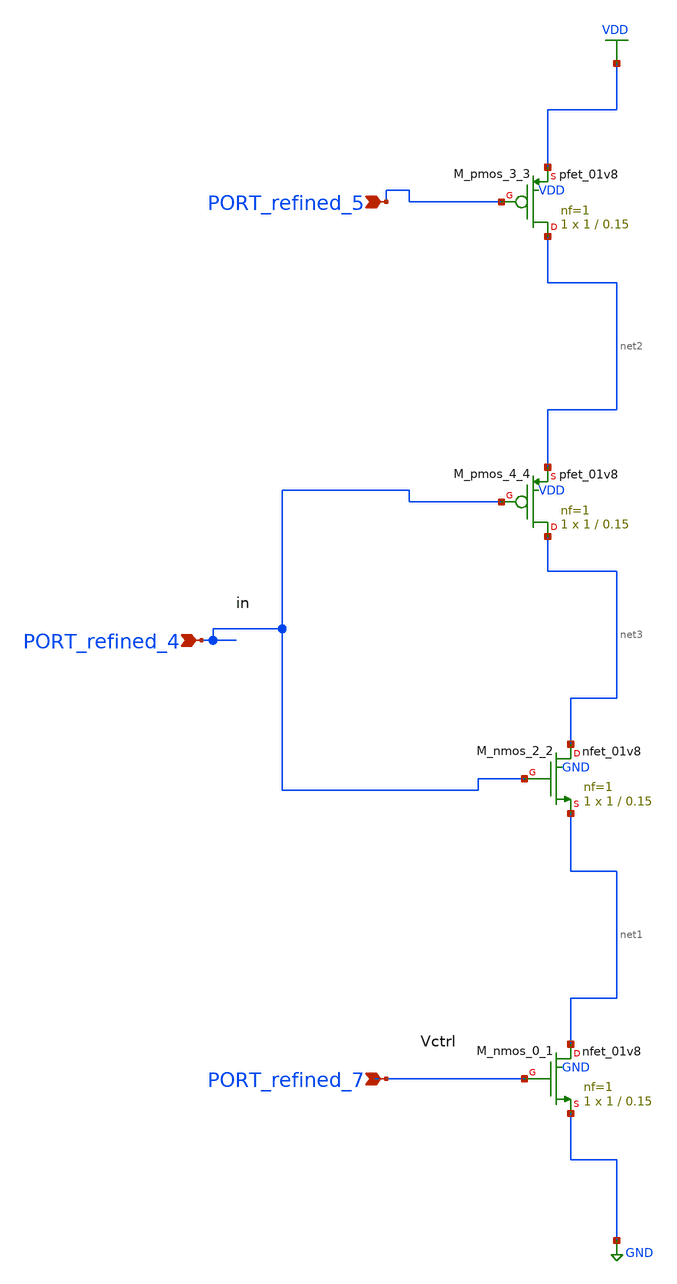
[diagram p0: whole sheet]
** sch_path: schematics/10_1109_ACCESS_2019_2905767_06_001_crop1.sch
**.subckt 10_1109_ACCESS_2019_2905767_06_001_crop1 PORT_refined_5 PORT_refined_4 PORT_refined_7
*.ipin PORT_refined_5
*.ipin PORT_refined_4
*.ipin PORT_refined_7
XM_nmos_0_1 net1 PORT_refined_7 GND GND sky130_fd_pr__nfet_01v8 L=0.15 W=1 nf=1 ad='int((1 + 1)/2) * 1 / 1 * 0.29'
+ as='int((1 + 2)/2) * 1 / 1 * 0.29' pd='2*int((1 + 1)/2) * (1 / 1 + 0.29)' ps='2*int((1 + 2)/2) * (1 / 1 + 0.29)'
+ nrd='0.29 / 1 ' nrs='0.29 / 1 ' sa=0 sb=0 sd=0 mult=1 m=1
XM_nmos_2_2 net3 PORT_refined_4 net1 GND sky130_fd_pr__nfet_01v8 L=0.15 W=1 nf=1 ad='int((1 + 1)/2) * 1 / 1 * 0.29'
+ as='int((1 + 2)/2) * 1 / 1 * 0.29' pd='2*int((1 + 1)/2) * (1 / 1 + 0.29)' ps='2*int((1 + 2)/2) * (1 / 1 + 0.29)'
+ nrd='0.29 / 1 ' nrs='0.29 / 1 ' sa=0 sb=0 sd=0 mult=1 m=1
XM_pmos_3_3 net2 PORT_refined_5 VDD VDD sky130_fd_pr__pfet_01v8 L=0.15 W=1 nf=1 ad='int((1 + 1)/2) * 1 / 1 * 0.29'
+ as='int((1 + 2)/2) * 1 / 1 * 0.29' pd='2*int((1 + 1)/2) * (1 / 1 + 0.29)' ps='2*int((1 + 2)/2) * (1 / 1 + 0.29)'
+ nrd='0.29 / 1 ' nrs='0.29 / 1 ' sa=0 sb=0 sd=0 mult=1 m=1
XM_pmos_4_4 net3 PORT_refined_4 net2 VDD sky130_fd_pr__pfet_01v8 L=0.15 W=1 nf=1 ad='int((1 + 1)/2) * 1 / 1 * 0.29'
+ as='int((1 + 2)/2) * 1 / 1 * 0.29' pd='2*int((1 + 1)/2) * (1 / 1 + 0.29)' ps='2*int((1 + 2)/2) * (1 / 1 + 0.29)'
+ nrd='0.29 / 1 ' nrs='0.29 / 1 ' sa=0 sb=0 sd=0 mult=1 m=1
**.ends
.GLOBAL GND
.GLOBAL VDD
.end
